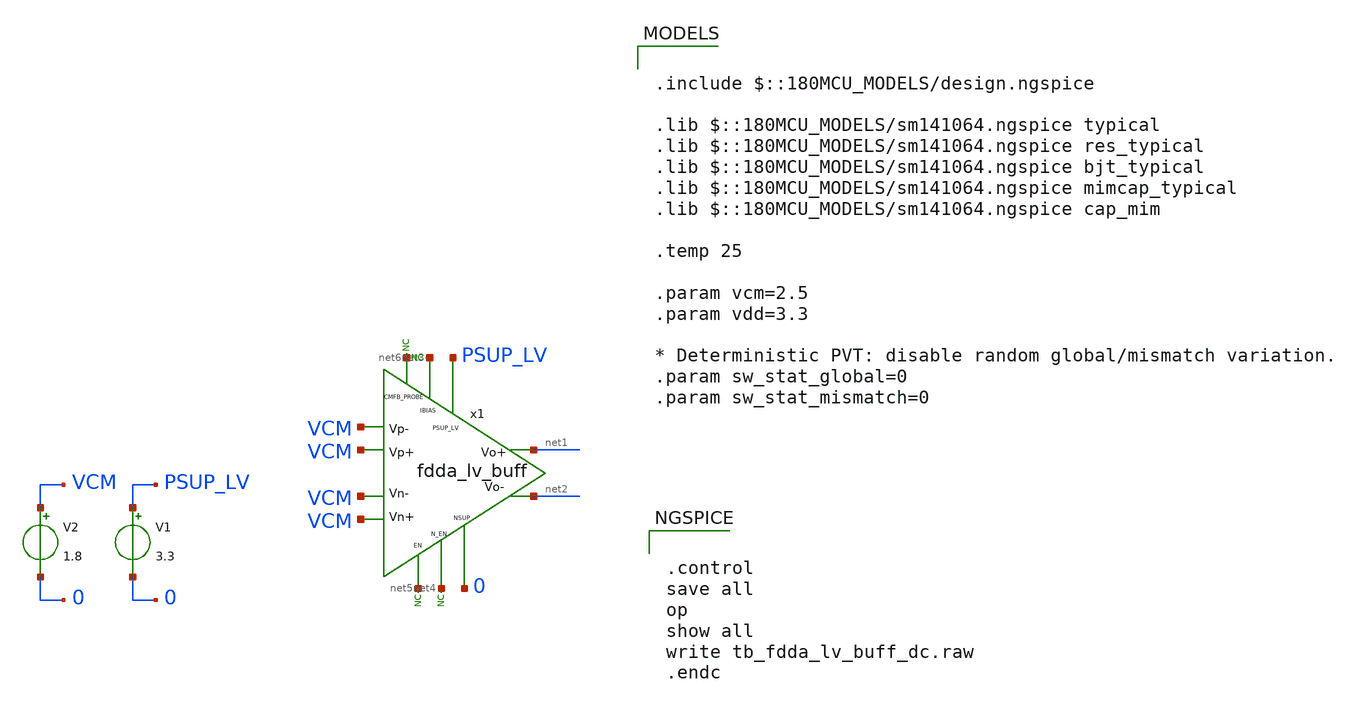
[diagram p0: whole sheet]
** sch_path: xschem/blocks/fdda_lv_buff/tb_fdda_lv_buff_dc.sch
**.subckt tb_fdda_lv_buff_dc
x1 PSUP_LV VCM VCM VCM VCM net1 net2 net3 net4 net5 0 net6 fdda_lv_buff
* noconn #net3
* noconn #net6
* noconn #net5
* noconn #net4
V1 PSUP_LV 0 3.3
V2 VCM 0 1.8
**** begin user architecture code


.control
save all
op
show all
write tb_fdda_lv_buff_dc.raw
.endc



.include $::180MCU_MODELS/design.ngspice

.lib $::180MCU_MODELS/sm141064.ngspice typical
.lib $::180MCU_MODELS/sm141064.ngspice res_typical
.lib $::180MCU_MODELS/sm141064.ngspice bjt_typical
.lib $::180MCU_MODELS/sm141064.ngspice mimcap_typical
.lib $::180MCU_MODELS/sm141064.ngspice cap_mim

.temp 25

.param vcm=2.5
.param vdd=3.3

* Deterministic PVT: disable random global/mismatch variation.
.param sw_stat_global=0
.param sw_stat_mismatch=0


**** end user architecture code
**.ends
.end
